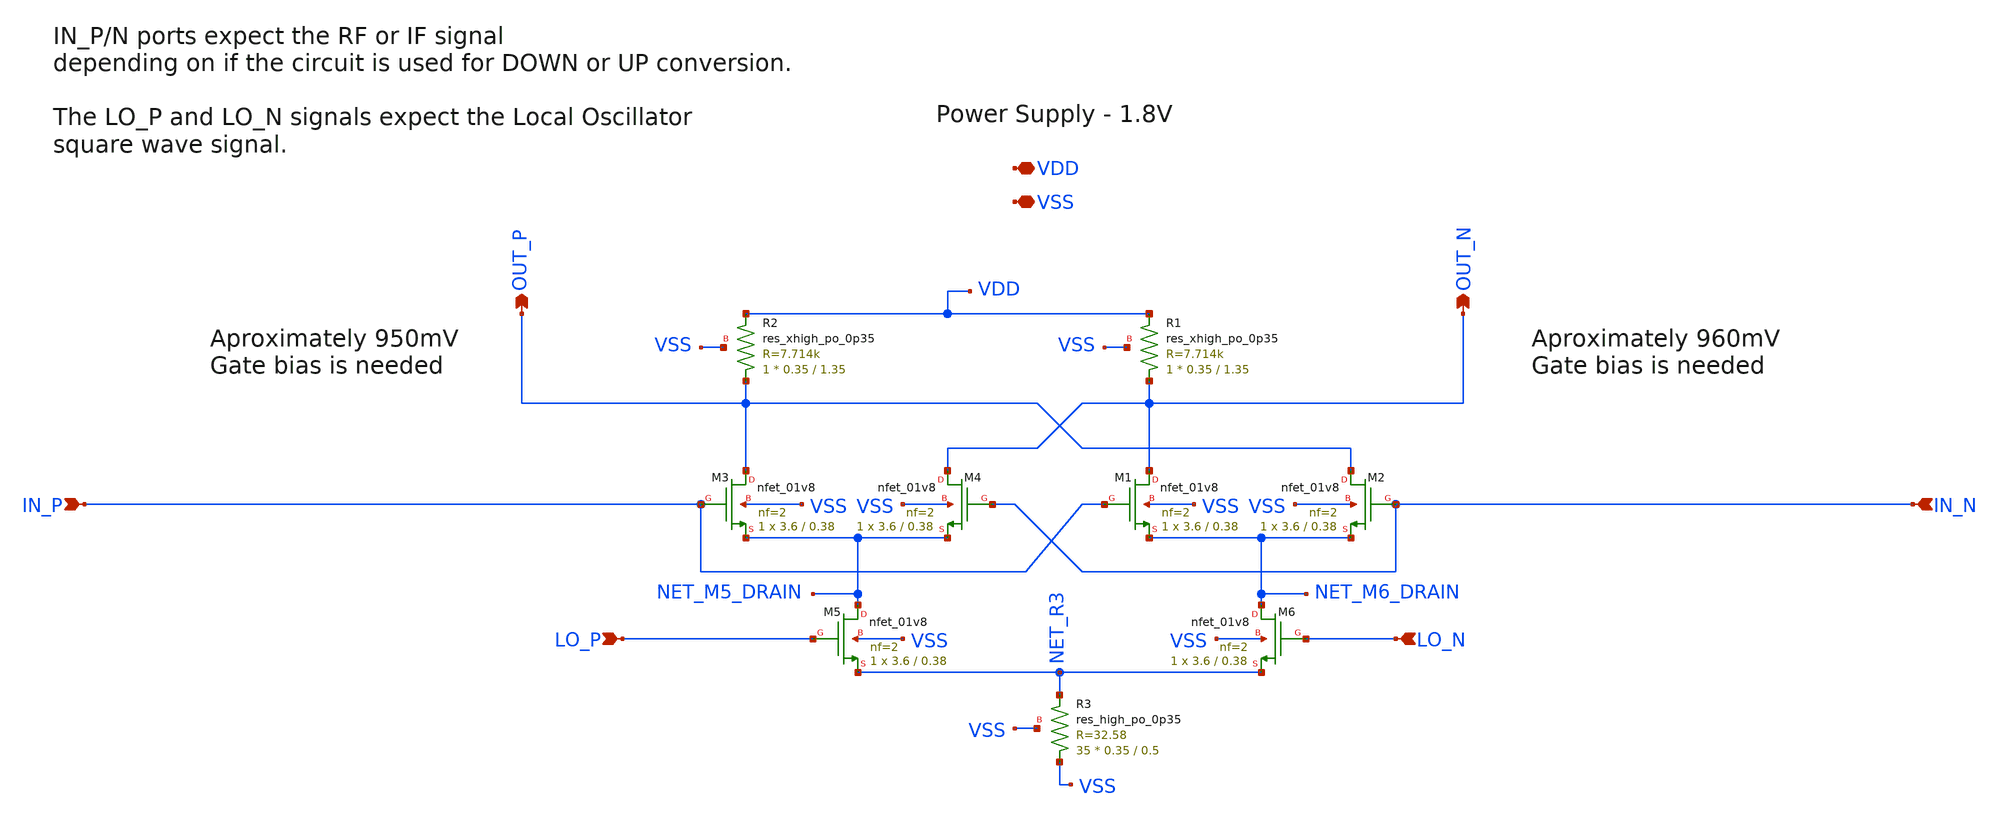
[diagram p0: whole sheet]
** sch_path: xschem/gilbert_mixer.sch
**.subckt gilbert_mixer LO_P LO_N IN_N OUT_N OUT_P VDD VSS IN_P
*.ipin LO_P
*.ipin LO_N
*.ipin IN_N
*.opin OUT_N
*.opin OUT_P
*.iopin VDD
*.iopin VSS
*.ipin IN_P
XR3 VSS NET_R3 VSS sky130_fd_pr__res_high_po_0p35 L=0.5 mult=35 m=35
XM2 OUT_P IN_N NET_M6_DRAIN VSS sky130_fd_pr__nfet_01v8 L=0.38 W=3.6 nf=2 ad='int((nf+1)/2) * W/nf * 0.29'
+ as='int((nf+2)/2) * W/nf * 0.29' pd='2*int((nf+1)/2) * (W/nf + 0.29)' ps='2*int((nf+2)/2) * (W/nf + 0.29)'
+ nrd='0.29 / W' nrs='0.29 / W' sa=0 sb=0 sd=0 mult=1 m=1
XM4 OUT_N IN_N NET_M5_DRAIN VSS sky130_fd_pr__nfet_01v8 L=0.38 W=3.6 nf=2 ad='int((nf+1)/2) * W/nf * 0.29'
+ as='int((nf+2)/2) * W/nf * 0.29' pd='2*int((nf+1)/2) * (W/nf + 0.29)' ps='2*int((nf+2)/2) * (W/nf + 0.29)'
+ nrd='0.29 / W' nrs='0.29 / W' sa=0 sb=0 sd=0 mult=1 m=1
XM6 NET_M6_DRAIN LO_N NET_R3 VSS sky130_fd_pr__nfet_01v8 L=0.38 W=3.6 nf=2 ad='int((nf+1)/2) * W/nf * 0.29'
+ as='int((nf+2)/2) * W/nf * 0.29' pd='2*int((nf+1)/2) * (W/nf + 0.29)' ps='2*int((nf+2)/2) * (W/nf + 0.29)'
+ nrd='0.29 / W' nrs='0.29 / W' sa=0 sb=0 sd=0 mult=1 m=1
XM1 OUT_N IN_P NET_M6_DRAIN VSS sky130_fd_pr__nfet_01v8 L=0.38 W=3.6 nf=2 ad='int((nf+1)/2) * W/nf * 0.29'
+ as='int((nf+2)/2) * W/nf * 0.29' pd='2*int((nf+1)/2) * (W/nf + 0.29)' ps='2*int((nf+2)/2) * (W/nf + 0.29)'
+ nrd='0.29 / W' nrs='0.29 / W' sa=0 sb=0 sd=0 mult=1 m=1
XM3 OUT_P IN_P NET_M5_DRAIN VSS sky130_fd_pr__nfet_01v8 L=0.38 W=3.6 nf=2 ad='int((nf+1)/2) * W/nf * 0.29'
+ as='int((nf+2)/2) * W/nf * 0.29' pd='2*int((nf+1)/2) * (W/nf + 0.29)' ps='2*int((nf+2)/2) * (W/nf + 0.29)'
+ nrd='0.29 / W' nrs='0.29 / W' sa=0 sb=0 sd=0 mult=1 m=1
XM5 NET_M5_DRAIN LO_P NET_R3 VSS sky130_fd_pr__nfet_01v8 L=0.38 W=3.6 nf=2 ad='int((nf+1)/2) * W/nf * 0.29'
+ as='int((nf+2)/2) * W/nf * 0.29' pd='2*int((nf+1)/2) * (W/nf + 0.29)' ps='2*int((nf+2)/2) * (W/nf + 0.29)'
+ nrd='0.29 / W' nrs='0.29 / W' sa=0 sb=0 sd=0 mult=1 m=1
XR1 OUT_N VDD VSS sky130_fd_pr__res_xhigh_po_0p35 L=1.35 mult=1 m=1
XR2 OUT_P VDD VSS sky130_fd_pr__res_xhigh_po_0p35 L=1.35 mult=1 m=1
**.ends
.end
